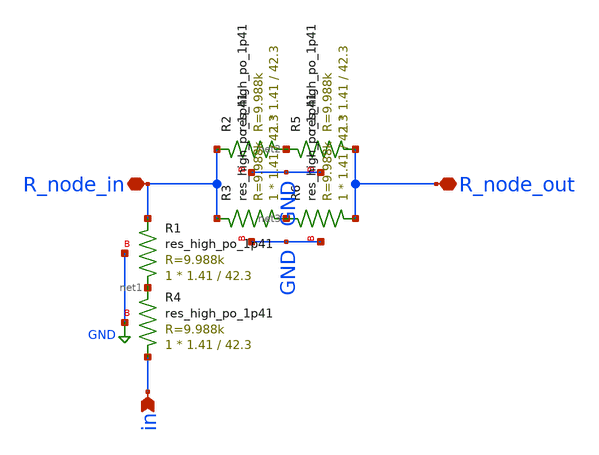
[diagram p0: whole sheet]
** sch_path: xschem/dac_sub_r2r.sch
**.subckt dac_sub_r2r in R_node_out R_node_in
*.ipin in
*.iopin R_node_out
*.iopin R_node_in
XR1 net1 R_node_in GND sky130_fd_pr__res_high_po_1p41 L=42.3 mult=1 m=1
XR2 net2 R_node_in GND sky130_fd_pr__res_high_po_1p41 L=42.3 mult=1 m=1
XR3 net3 R_node_in GND sky130_fd_pr__res_high_po_1p41 L=42.3 mult=1 m=1
XR4 in net1 GND sky130_fd_pr__res_high_po_1p41 L=42.3 mult=1 m=1
XR5 R_node_out net2 GND sky130_fd_pr__res_high_po_1p41 L=42.3 mult=1 m=1
XR6 R_node_out net3 GND sky130_fd_pr__res_high_po_1p41 L=42.3 mult=1 m=1
**.ends
.GLOBAL GND
.end
